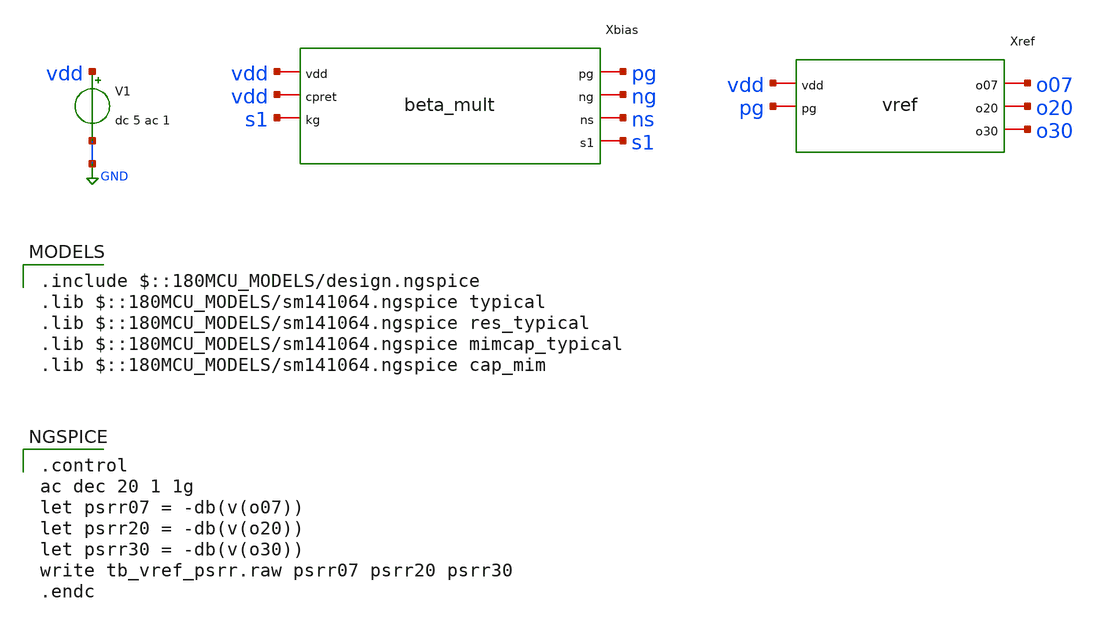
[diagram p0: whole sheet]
** sch_path: schematic pt2/sims/tb/tb_vref_psrr.sch
**.subckt tb_vref_psrr
V1 vdd GND dc 5 ac 1
Xbias vdd pg ng ns vdd s1 s1 beta_mult
Xref vdd pg o07 o20 o30 vref
**** begin user architecture code
 .include $::180MCU_MODELS/design.ngspice
.lib $::180MCU_MODELS/sm141064.ngspice typical
.lib $::180MCU_MODELS/sm141064.ngspice res_typical
.lib $::180MCU_MODELS/sm141064.ngspice mimcap_typical
.lib $::180MCU_MODELS/sm141064.ngspice cap_mim

.control
ac dec 20 1 1g
let psrr07 = -db(v(o07))
let psrr20 = -db(v(o20))
let psrr30 = -db(v(o30))
write tb_vref_psrr.raw psrr07 psrr20 psrr30
.endc

**** end user architecture code
**.ends
.GLOBAL GND
.end
